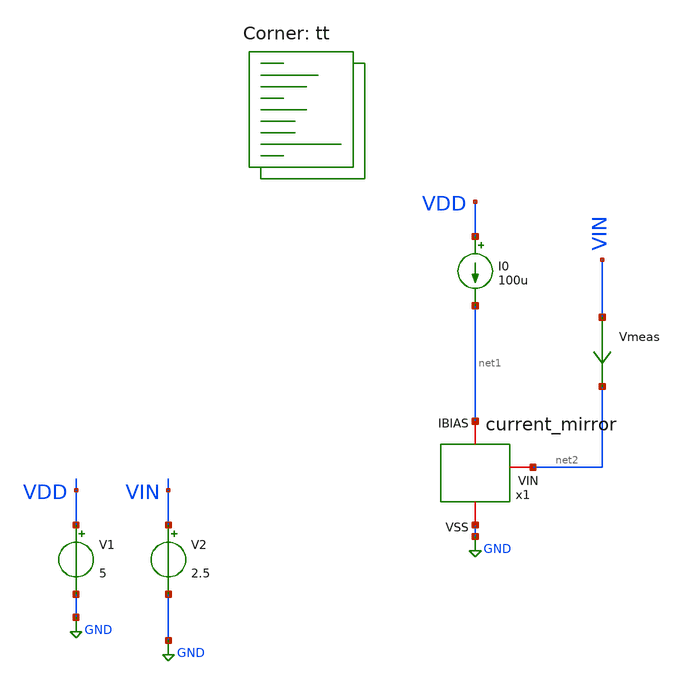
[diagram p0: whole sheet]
** sch_path: old stuff/amplifiers/current_mirrors/cascode_current_mirror/current_mirror_test.sch
**.subckt current_mirror_test
V1 VDD GND 5
V2 VIN GND 2.5
I0 VDD net1 100u
Vmeas VIN net2 0
.save i(vmeas)
x1 net1 GND net2 current_mirror
**** begin user architecture code

**************************************************************
**************************************************************
**************************************************************
**************************************************************
**************************************************************
*LIBs*********************************************************
**************************************************************
**************************************************************
**************************************************************
**************************************************************
**************************************************************
*.lib $::SKYWATER_MODELS/sky130.lib.spice tt
* chose the corners in the corner file
* tt_mm for mismatch
* ss ff sf fs standart corners
* ll hh lh hl capacitor and resistors corners
* mc for total process variation including corners
**************************************************************
**************************************************************
**************************************************************
**************************************************************
**************************************************************
*Corners/montecarlo options***********************************
**************************************************************
**************************************************************
**************************************************************
**************************************************************
**************************************************************
.TEMP 27
**************************************************************
**************************************************************
**************************************************************
**************************************************************
*SIMULATION and Plots*****************************************
**************************************************************
**************************************************************
**************************************************************
**************************************************************
.control
save all
dc V2 0 5 0.001
*dc simulation
*ploting VIN VOUT and the voltage gain
plot i(Vmeas)
plot 1/deriv(i(Vmeas))
.endc

.lib $::SKYWATER_MODELS/sky130.lib.spice tt
**** end user architecture code
**.ends

* expanding   symbol:
*+  /home/vasco/Desktop/sky130A/amplifiers/current_mirrors/cascode_current_mirror/current_mirror.sym # of pins=3
** sym_path: amplifiers/current_mirrors/lower_vt_current_mirror/current_mirror.sym
** sch_path: amplifiers/current_mirrors/lower_vt_current_mirror/current_mirror.sch
.subckt current_mirror IBIAS VSS VIN
*.iopin IBIAS
*.iopin VSS
*.iopin VIN
XM5 net1 IBIAS VSS VSS sky130_fd_pr__nfet_g5v0d10v5 L=0.7 W=50 nf=1 ad='int((1 + 1)/2) * 50 / 1 * 0.29'
+ as='int((1 + 2)/2) * 50 / 1 * 0.29' pd='2*int((1 + 1)/2) * (50 / 1 + 0.29)' ps='2*int((1 + 2)/2) * (50 / 1 + 0.29)'
+ nrd='0.29 / 50 ' nrs='0.29 / 50 ' sa=0 sb=0 sd=0 mult=1 m=1
XM1 net2 IBIAS VSS VSS sky130_fd_pr__nfet_g5v0d10v5 L=0.7 W=50 nf=1 ad='int((1 + 1)/2) * 50 / 1 * 0.29'
+ as='int((1 + 2)/2) * 50 / 1 * 0.29' pd='2*int((1 + 1)/2) * (50 / 1 + 0.29)' ps='2*int((1 + 2)/2) * (50 / 1 + 0.29)'
+ nrd='0.29 / 50 ' nrs='0.29 / 50 ' sa=0 sb=0 sd=0 mult=1 m=1
XM2 IBIAS VB1 net1 VSS sky130_fd_pr__nfet_g5v0d10v5 L=0.7 W=50 nf=1 ad='int((1 + 1)/2) * 50 / 1 * 0.29'
+ as='int((1 + 2)/2) * 50 / 1 * 0.29' pd='2*int((1 + 1)/2) * (50 / 1 + 0.29)' ps='2*int((1 + 2)/2) * (50 / 1 + 0.29)'
+ nrd='0.29 / 50 ' nrs='0.29 / 50 ' sa=0 sb=0 sd=0 mult=1 m=1
XM3 VIN VB1 net2 VSS sky130_fd_pr__nfet_g5v0d10v5 L=0.7 W=50 nf=1 ad='int((1 + 1)/2) * 50 / 1 * 0.29'
+ as='int((1 + 2)/2) * 50 / 1 * 0.29' pd='2*int((1 + 1)/2) * (50 / 1 + 0.29)' ps='2*int((1 + 2)/2) * (50 / 1 + 0.29)'
+ nrd='0.29 / 50 ' nrs='0.29 / 50 ' sa=0 sb=0 sd=0 mult=1 m=1
I0 net3 VB1 200u
V1 net3 VSS 5
XM4 VB1 VB1 net4 VSS sky130_fd_pr__nfet_g5v0d10v5 L=2 W=10 nf=1 ad='int((1 + 1)/2) * 10 / 1 * 0.29' as='int((1 + 2)/2) * 10 / 1 * 0.29'
+ pd='2*int((1 + 1)/2) * (10 / 1 + 0.29)' ps='2*int((1 + 2)/2) * (10 / 1 + 0.29)' nrd='0.29 / 10 ' nrs='0.29 / 10 '
+ sa=0 sb=0 sd=0 mult=1 m=1
XM6 net4 VB1 VSS VSS sky130_fd_pr__nfet_g5v0d10v5 L=2 W=10 nf=1 ad='int((1 + 1)/2) * 10 / 1 * 0.29' as='int((1 + 2)/2) * 10 / 1 * 0.29'
+ pd='2*int((1 + 1)/2) * (10 / 1 + 0.29)' ps='2*int((1 + 2)/2) * (10 / 1 + 0.29)' nrd='0.29 / 10 ' nrs='0.29 / 10 '
+ sa=0 sb=0 sd=0 mult=1 m=1
.ends

.GLOBAL GND
.end
